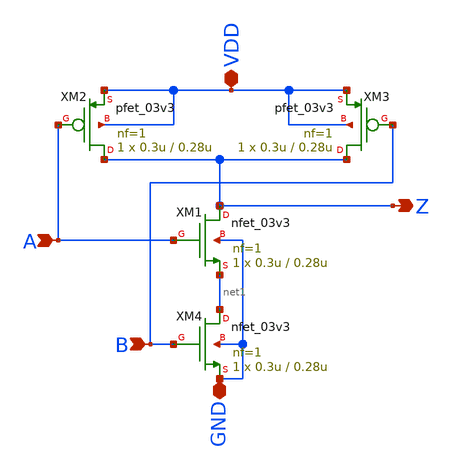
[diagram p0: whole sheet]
** sch_path: pll_block_templates_v1/layout2/nand.sch
**.subckt nand A VDD Z GND B
*.ipin A
*.iopin VDD
*.opin Z
*.iopin GND
*.ipin B
XM1 Z A net1 GND nfet_03v3 L=0.28u W=0.3u nf=1 ad='int((nf+1)/2) * W/nf * 0.18u' as='int((nf+2)/2) * W/nf * 0.18u'
+ pd='2*int((nf+1)/2) * (W/nf + 0.18u)' ps='2*int((nf+2)/2) * (W/nf + 0.18u)' nrd='0.18u / W' nrs='0.18u / W'
+ sa=0 sb=0 sd=0 m=1
XM2 Z A VDD VDD pfet_03v3 L=0.28u W=0.3u nf=1 ad='int((nf+1)/2) * W/nf * 0.18u' as='int((nf+2)/2) * W/nf * 0.18u'
+ pd='2*int((nf+1)/2) * (W/nf + 0.18u)' ps='2*int((nf+2)/2) * (W/nf + 0.18u)' nrd='0.18u / W' nrs='0.18u / W'
+ sa=0 sb=0 sd=0 m=1
XM3 Z B VDD VDD pfet_03v3 L=0.28u W=0.3u nf=1 ad='int((nf+1)/2) * W/nf * 0.18u' as='int((nf+2)/2) * W/nf * 0.18u'
+ pd='2*int((nf+1)/2) * (W/nf + 0.18u)' ps='2*int((nf+2)/2) * (W/nf + 0.18u)' nrd='0.18u / W' nrs='0.18u / W'
+ sa=0 sb=0 sd=0 m=1
XM4 net1 B GND GND nfet_03v3 L=0.28u W=0.3u nf=1 ad='int((nf+1)/2) * W/nf * 0.18u' as='int((nf+2)/2) * W/nf * 0.18u'
+ pd='2*int((nf+1)/2) * (W/nf + 0.18u)' ps='2*int((nf+2)/2) * (W/nf + 0.18u)' nrd='0.18u / W' nrs='0.18u / W'
+ sa=0 sb=0 sd=0 m=1
**.ends
.end
